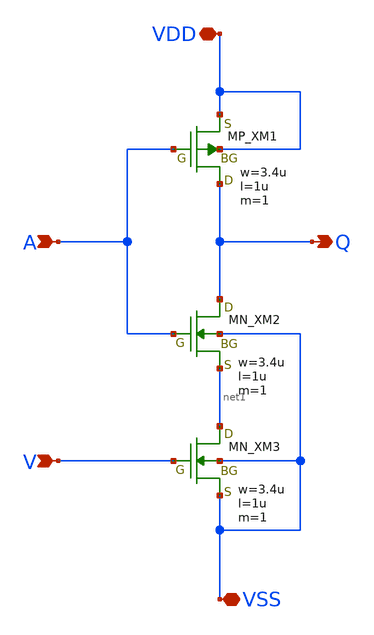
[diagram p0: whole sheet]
** sch_path: src/csi.sch
**.subckt csi A Q VDD VSS V
*.ipin A
*.opin Q
*.iopin VDD
*.iopin VSS
*.ipin V
XXM1 Q A VDD VDD PMOS w=3.4u l=1u as=0 ad=0 ps=0 pd=0 nrd=0 nrs=0 m=1
XXM2 Q A net1 VSS NMOS w=3.4u l=1u as=0 ad=0 ps=0 pd=0 nrd=0 nrs=0 m=1
XXM3 net1 V VSS VSS NMOS w=3.4u l=1u as=0 ad=0 ps=0 pd=0 nrd=0 nrs=0 m=1
**.ends
.end
